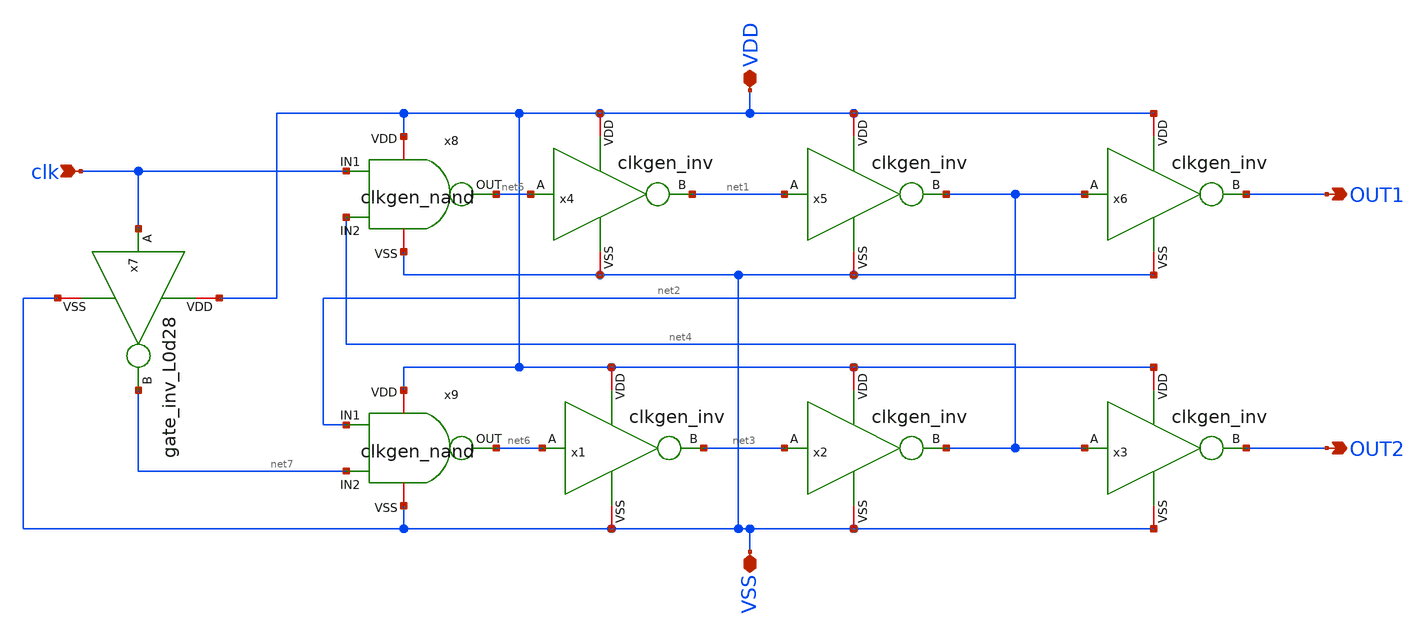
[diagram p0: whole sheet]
** sch_path: designs/DS_modulator/clkgen/xscheme/clkgen.sch
**.subckt clkgen clk OUT1 OUT2 VDD VSS
*.ipin clk
*.opin OUT1
*.opin OUT2
*.iopin VDD
*.iopin VSS
x7 VDD net7 clk VSS gate_inv_L0d28
x1 VDD net3 net6 VSS clkgen_inv
x2 VDD net4 net3 VSS clkgen_inv
x3 VDD OUT2 net4 VSS clkgen_inv
x6 VDD OUT1 net2 VSS clkgen_inv
x4 VDD net1 net5 VSS clkgen_inv
x5 VDD net2 net1 VSS clkgen_inv
x8 VDD clk net5 net4 VSS clkgen_nand
x9 VDD net2 net6 net7 VSS clkgen_nand
**.ends

* expanding   symbol:
*+  chipaton/chipa2026_gf180mcu_DeltaSigma/designs/DS_modulator/gate_inv_L0d28/xschem/gate_inv_L0d28.sym # of pins=4
** sym_path: chipaton/chipa2026_gf180mcu_DeltaSigma/designs/DS_modulator/gate_inv_L0d28/xschem/gate_inv_L0d28.sym
** sch_path: chipaton/chipa2026_gf180mcu_DeltaSigma/designs/DS_modulator/gate_inv_L0d28/xschem/gate_inv_L0d28.sch
.subckt gate_inv_L0d28 VDD B A VSS
*.opin B
*.ipin A
*.iopin VDD
*.iopin VSS
XMN B A VSS VSS nfet_03v3 L=0.28u W=1u nf=1 ad='int((nf+1)/2) * W/nf * 0.18u' as='int((nf+2)/2) * W/nf * 0.18u'
+ pd='2*int((nf+1)/2) * (W/nf + 0.18u)' ps='2*int((nf+2)/2) * (W/nf + 0.18u)' nrd='0.18u / W' nrs='0.18u / W'
+ sa=0 sb=0 sd=0 m=2
XMP B A VDD VDD pfet_03v3 L=0.28u W=3u nf=1 ad='int((nf+1)/2) * W/nf * 0.18u' as='int((nf+2)/2) * W/nf * 0.18u'
+ pd='2*int((nf+1)/2) * (W/nf + 0.18u)' ps='2*int((nf+2)/2) * (W/nf + 0.18u)' nrd='0.18u / W' nrs='0.18u / W'
+ sa=0 sb=0 sd=0 m=2
.ends


* expanding   symbol:
*+  chipaton/chipa2026_gf180mcu_DeltaSigma/designs/DS_modulator/clkgen_inv/xscheme/clkgen_inv.sym # of pins=4
** sym_path: designs/DS_modulator/clkgen_inv/xscheme/clkgen_inv.sym
** sch_path: designs/DS_modulator/clkgen_inv/xscheme/clkgen_inv.sch
.subckt clkgen_inv VDD B A VSS
*.opin B
*.ipin A
*.iopin VDD
*.iopin VSS
XMN B A VSS VSS nfet_03v3 L=0.28u W=1.8u nf=1 ad='int((nf+1)/2) * W/nf * 0.18u' as='int((nf+2)/2) * W/nf * 0.18u'
+ pd='2*int((nf+1)/2) * (W/nf + 0.18u)' ps='2*int((nf+2)/2) * (W/nf + 0.18u)' nrd='0.18u / W' nrs='0.18u / W'
+ sa=0 sb=0 sd=0 m=4
XMP B A VDD VDD pfet_03v3 L=0.28u W=1.8u nf=1 ad='int((nf+1)/2) * W/nf * 0.18u' as='int((nf+2)/2) * W/nf * 0.18u'
+ pd='2*int((nf+1)/2) * (W/nf + 0.18u)' ps='2*int((nf+2)/2) * (W/nf + 0.18u)' nrd='0.18u / W' nrs='0.18u / W'
+ sa=0 sb=0 sd=0 m=8
.ends


* expanding   symbol:
*+  chipaton/chipa2026_gf180mcu_DeltaSigma/designs/DS_modulator/clkgen_nand/xscheme/clkgen_nand.sym # of pins=5
** sym_path: chipaton/chipa2026_gf180mcu_DeltaSigma/designs/DS_modulator/clkgen_nand/xscheme/clkgen_nand.sym
** sch_path: chipaton/chipa2026_gf180mcu_DeltaSigma/designs/DS_modulator/clkgen_nand/xscheme/clkgen_nand.sch
.subckt clkgen_nand VDD IN1 OUT IN2 VSS
*.ipin IN1
*.opin OUT
*.iopin VDD
*.ipin IN2
*.iopin VSS
XM1 net1 IN2 VSS VSS nfet_03v3 L=0.28u W=0.22u nf=1 ad='int((nf+1)/2) * W/nf * 0.18u' as='int((nf+2)/2) * W/nf * 0.18u'
+ pd='2*int((nf+1)/2) * (W/nf + 0.18u)' ps='2*int((nf+2)/2) * (W/nf + 0.18u)' nrd='0.18u / W' nrs='0.18u / W'
+ sa=0 sb=0 sd=0 m=1
XM2 OUT IN1 net1 VSS nfet_03v3 L=0.28u W=0.22u nf=1 ad='int((nf+1)/2) * W/nf * 0.18u' as='int((nf+2)/2) * W/nf * 0.18u'
+ pd='2*int((nf+1)/2) * (W/nf + 0.18u)' ps='2*int((nf+2)/2) * (W/nf + 0.18u)' nrd='0.18u / W' nrs='0.18u / W'
+ sa=0 sb=0 sd=0 m=1
XM3 OUT IN1 VDD VDD pfet_03v3 L=0.28u W=0.22u nf=1 ad='int((nf+1)/2) * W/nf * 0.18u' as='int((nf+2)/2) * W/nf * 0.18u'
+ pd='2*int((nf+1)/2) * (W/nf + 0.18u)' ps='2*int((nf+2)/2) * (W/nf + 0.18u)' nrd='0.18u / W' nrs='0.18u / W'
+ sa=0 sb=0 sd=0 m=1
XM5 OUT IN2 VDD VDD pfet_03v3 L=0.28u W=0.22u nf=1 ad='int((nf+1)/2) * W/nf * 0.18u' as='int((nf+2)/2) * W/nf * 0.18u'
+ pd='2*int((nf+1)/2) * (W/nf + 0.18u)' ps='2*int((nf+2)/2) * (W/nf + 0.18u)' nrd='0.18u / W' nrs='0.18u / W'
+ sa=0 sb=0 sd=0 m=1
.ends

.end
